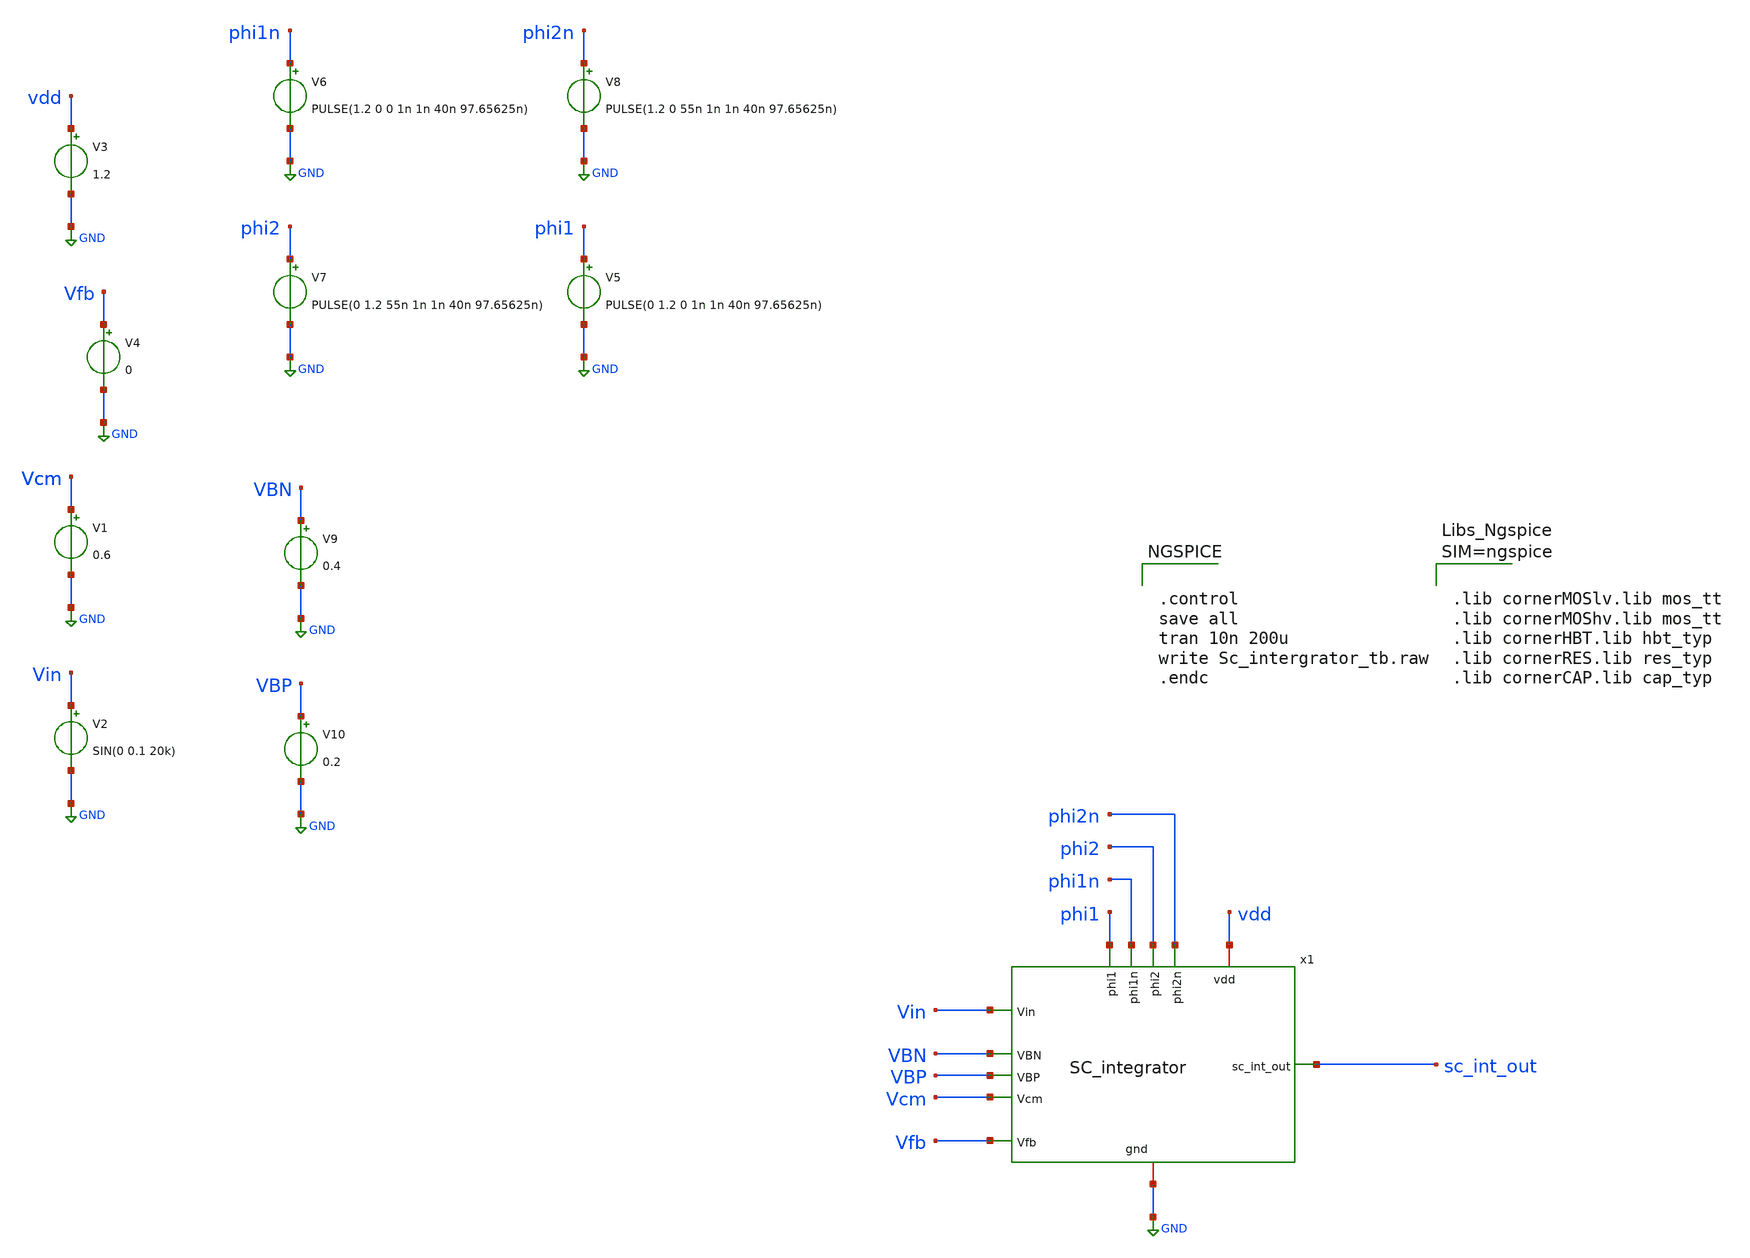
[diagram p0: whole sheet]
** sch_path: xschem/SC_intergrator_tb2.sch
**.subckt SC_intergrator_tb2
V1 Vcm GND 0.6
V2 Vin GND SIN(0 0.1 20k)
V3 vdd GND 1.2
V9 VBN GND 0.4
V10 VBP GND 0.2
V4 Vfb GND 0
V5 phi1 GND PULSE(0 1.2 0 1n 1n 40n 97.65625n)
V6 phi1n GND PULSE(1.2 0 0 1n 1n 40n 97.65625n)
V7 phi2 GND PULSE(0 1.2 55n 1n 1n 40n 97.65625n)
V8 phi2n GND PULSE(1.2 0 55n 1n 1n 40n 97.65625n)
x1 Vin Vfb phi1 phi1n phi2 phi2n VBN VBP vdd GND sc_int_out Vcm SC_integrator
**** begin user architecture code


.control
save all
tran 10n 200u
write Sc_intergrator_tb.raw
.endc





.lib cornerMOSlv.lib mos_tt
.lib cornerMOShv.lib mos_tt
.lib cornerHBT.lib hbt_typ
.lib cornerRES.lib res_typ
.lib cornerCAP.lib cap_typ



**** end user architecture code
**.ends

* expanding   symbol:  SC_integrator.sym # of pins=12
** sym_path: xschem/SC_integrator.sym
** sch_path: xschem/SC_integrator.sch
.subckt SC_integrator Vin Vfb phi1 phi1n phi2 phi2n VBN VBP vdd gnd sc_int_out Vcm
*.ipin Vin
*.ipin Vfb
*.ipin phi1
*.ipin phi1n
*.ipin phi2
*.ipin phi2n
*.ipin VBN
*.ipin VBP
*.iopin vdd
*.iopin gnd
*.opin sc_int_out
*.ipin Vcm
x1 Vin phi1 phi1n Vfb phi2 phi2n Vcm net1 vdd gnd switched_capacitor
x5 net1 Vcm VBN VBP sc_int_out vdd gnd Pseudo_compensated_self_cascode_OTA
XC2 net1 sc_int_out cap_cmim w=5.0e-6 l=5.0e-6 m=25 mm_ok=1
XC1 sc_int_out gnd cap_cmim w=5.0e-6 l=5.0e-6 m=53 mm_ok=1
.ends


* expanding   symbol:  switched_capacitor.sym # of pins=10
** sym_path: xschem/switched_capacitor.sym
** sch_path: xschem/switched_capacitor.sch
.subckt switched_capacitor Vin phi1 phi1n Vfb phi2 phi2n Vcm vout vdd gnd
*.ipin Vin
*.ipin phi1
*.ipin phi1n
*.ipin Vfb
*.ipin phi2
*.ipin phi2n
*.ipin Vcm
*.opin vout
*.iopin vdd
*.iopin gnd
x1 phi1n Vin sc_left gnd phi1 vdd T_gate
x2 phi2n Vfb sc_left gnd phi2 vdd T_gate
x3 phi1n Vcm sc_right gnd phi1 vdd T_gate
XC1 sc_left sc_right cap_cmim w=5.0e-6 l=5.0e-6 m=50 mm_ok=1
x4 phi2n sc_right vout gnd phi2 vdd T_gate
XC4 vout gnd cap_cmim w=5.0e-6 l=5.0e-6 m=100 mm_ok=1
.ends


* expanding   symbol:  Pseudo_compensated_self_cascode_OTA.sym # of pins=7
** sym_path: xschem/Pseudo_compensated_self_cascode_OTA.sym
** sch_path: xschem/Pseudo_compensated_self_cascode_OTA.sch
.subckt Pseudo_compensated_self_cascode_OTA VN VP V_BN V_BP V_OUT VDD VSS
*.ipin VN
*.ipin VP
*.ipin V_BN
*.ipin V_BP
*.opin V_OUT
*.iopin VDD
*.iopin VSS
XM11 net1 VN net2 VSS sg13_lv_nmos w=70u l=0.8u ng=7 m=1 mm_ok=1
XM12 V_GS VN net1 V_BP sg13_lv_nmos w=38.5u l=0.3u ng=4 m=1 mm_ok=1
XM21 net4 VP net2 VSS sg13_lv_nmos w=70u l=0.8u ng=7 m=1 mm_ok=1
XM22 VB32 VP net4 V_BP sg13_lv_nmos w=38.5u l=0.3u ng=4 m=1 mm_ok=1
XM52 net2 V_BN net3 V_BN sg13_lv_nmos w=40u l=0.5u ng=4 m=1 mm_ok=1
XM51 net3 V_BN VSS VSS sg13_lv_nmos w=40u l=2.5u ng=4 m=1 mm_ok=1
XM32 V_GS V_GS VS32 VB32 sg13_lv_pmos w=48.5u l=1.24u ng=5 m=1 mm_ok=1
XM31 VS32 V_GS VDD VDD sg13_lv_pmos w=48.5u l=0.87u ng=5 m=1 mm_ok=1
XM42 VB32 V_GS VS42 V_GS sg13_lv_pmos w=48.5u l=1.24u ng=5 m=1 mm_ok=1
XM41 VS42 V_GS VDD VDD sg13_lv_pmos w=48.5u l=0.87u ng=5 m=1 mm_ok=1
XM61 net5 VB32 VDD VDD sg13_lv_pmos w=60u l=0.13u ng=6 m=1 mm_ok=1
XM62 V_OUT VB32 net5 V_BP sg13_lv_pmos w=60u l=0.13u ng=6 m=1 mm_ok=1
XM72 V_OUT V_BN net6 V_BN sg13_lv_nmos w=40u l=0.5u ng=10 m=1 mm_ok=1
XM71 net6 V_BN VSS VSS sg13_lv_nmos w=40u l=2.5u ng=4 m=1 mm_ok=1
XC3 VS42 V_OUT cap_cmim w=5.0e-6 l=5.0e-6 m=38 mm_ok=1
XC1 net4 V_OUT cap_cmim w=5.0e-6 l=5.0e-6 m=38 mm_ok=1
.ends


* expanding   symbol:  T_gate.sym # of pins=6
** sym_path: T_gate.sym
** sch_path: T_gate.sch
.subckt T_gate !Control Vin Vout gnd Control vdd
*.iopin Vout
*.iopin Vin
*.iopin !Control
*.iopin Control
*.iopin gnd
*.iopin vdd
XM1 Vin Control Vout gnd sg13_lv_nmos w=1u l=0.13u ng=1 m=1 mm_ok=1
XM2 Vout !Control Vin vdd sg13_lv_pmos w=3u l=0.13u ng=1 m=1 mm_ok=1
.ends

.GLOBAL GND
.end
